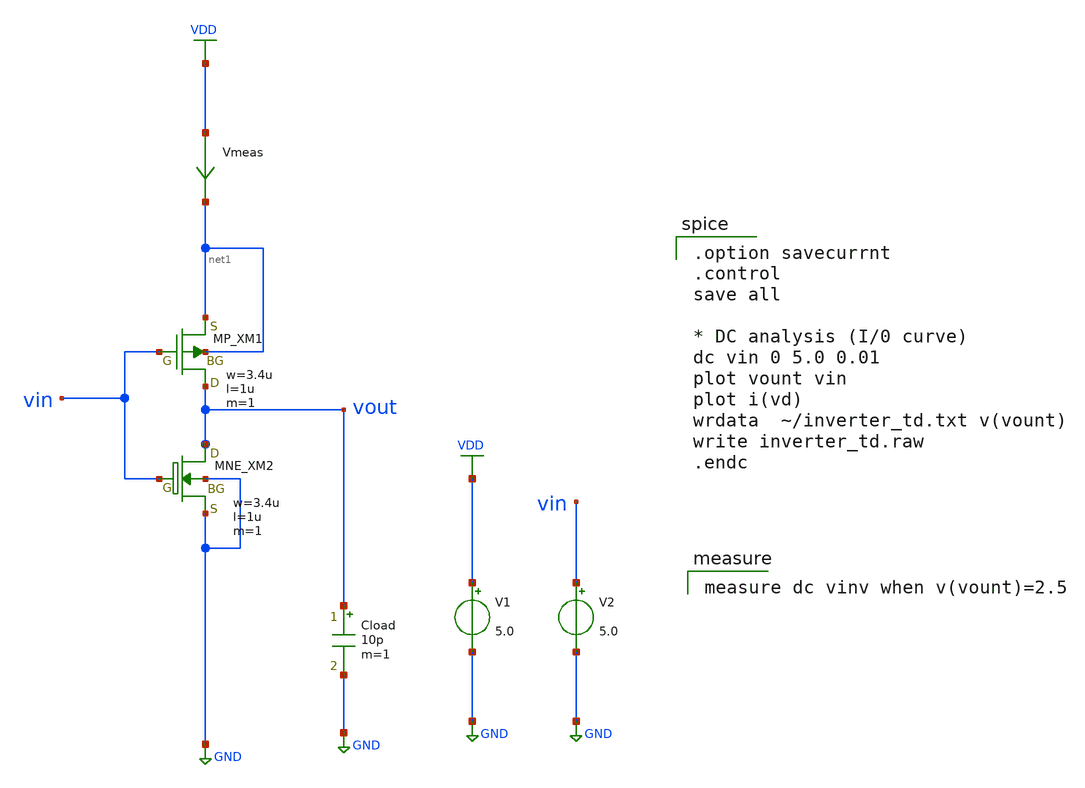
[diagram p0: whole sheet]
** sch_path: inverter/inverter_Tanaka_Airi_tb.sch
**.subckt inverter_Tanaka_Airi_tb
XXM1 vout vin net1 net1 PMOS w=3.4u l=1u nrd=0 nrs=0 m=1
XXM2 vout vin GND GND MNE w=3.4u l=1u as=0 ad=0 ps=0 pd=0 nrd=0 nrs=0 m=1
V1 VDD GND 5.0
V2 vin GND 5.0
Cload vout GND 10p m=1
Vmeas VDD net1 0
.save i(vmeas)
**** begin user architecture code

.option savecurrnt
.control
save all

* DC analysis (I/0 curve)
dc vin 0 5.0 0.01
plot vount vin
plot i(vd)
wrdata  ~/inverter_td.txt v(vount)
write inverter_td.raw
.endc


blabla


measure dc vinv when v(vount)=2.5

**** end user architecture code
**.ends
.GLOBAL GND
.GLOBAL VDD
.end
